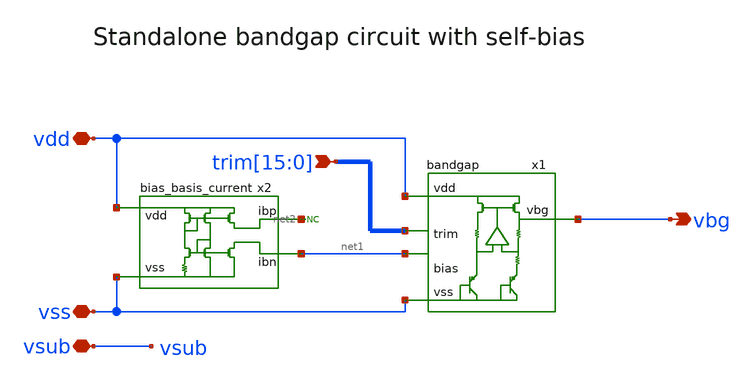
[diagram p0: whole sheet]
** sch_path: xschem/sky130_cw_ip__bandgap.sch
**.subckt sky130_cw_ip__bandgap vsub vss vdd vbg
*+ trim[15],trim[14],trim[13],trim[12],trim[11],trim[10],trim[9],trim[8],trim[7],trim[6],trim[5],trim[4],trim[3],trim[2],trim[1],trim[0]
*.iopin vsub
*.iopin vss
*.iopin vdd
*.opin vbg
*.ipin
*+ trim[15],trim[14],trim[13],trim[12],trim[11],trim[10],trim[9],trim[8],trim[7],trim[6],trim[5],trim[4],trim[3],trim[2],trim[1],trim[0]
x1 vdd vbg vss net1 trim[15] trim[14] trim[13] trim[12] trim[11] trim[10] trim[9] trim[8] trim[7]
+ trim[6] trim[5] trim[4] trim[3] trim[2] trim[1] trim[0] bandgap
x2 vdd vss net2 net1 bias_basis_current
* noconn #net2
**.ends
.end
